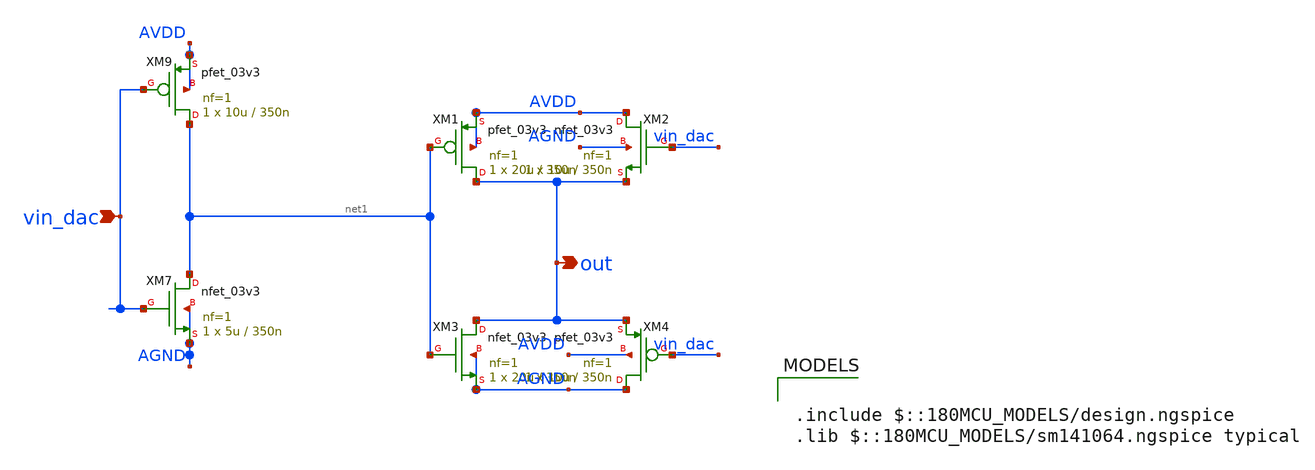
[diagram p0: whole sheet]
** sch_path: untitled.sch
**.subckt untitled vin_dac out
*.ipin vin_dac
*.opin out
XM7 net1 vin_dac AGND AGND nfet_03v3 L=350n W=5u nf=1 ad='int((nf+1)/2) * W/nf * 0.18u' as='int((nf+2)/2) * W/nf * 0.18u'
+ pd='2*int((nf+1)/2) * (W/nf + 0.18u)' ps='2*int((nf+2)/2) * (W/nf + 0.18u)' nrd='0.18u / W' nrs='0.18u / W'
+ sa=0 sb=0 sd=0 m=1
XM9 net1 vin_dac AVDD AVDD pfet_03v3 L=350n W=10u nf=1 ad='int((nf+1)/2) * W/nf * 0.18u' as='int((nf+2)/2) * W/nf * 0.18u'
+ pd='2*int((nf+1)/2) * (W/nf + 0.18u)' ps='2*int((nf+2)/2) * (W/nf + 0.18u)' nrd='0.18u / W' nrs='0.18u / W'
+ sa=0 sb=0 sd=0 m=1
XM1 out net1 AVDD AVDD pfet_03v3 L=350n W=20u nf=1 ad='int((nf+1)/2) * W/nf * 0.18u' as='int((nf+2)/2) * W/nf * 0.18u'
+ pd='2*int((nf+1)/2) * (W/nf + 0.18u)' ps='2*int((nf+2)/2) * (W/nf + 0.18u)' nrd='0.18u / W' nrs='0.18u / W'
+ sa=0 sb=0 sd=0 m=1
XM2 AVDD vin_dac out AGND nfet_03v3 L=350n W=10u nf=1 ad='int((nf+1)/2) * W/nf * 0.18u' as='int((nf+2)/2) * W/nf * 0.18u'
+ pd='2*int((nf+1)/2) * (W/nf + 0.18u)' ps='2*int((nf+2)/2) * (W/nf + 0.18u)' nrd='0.18u / W' nrs='0.18u / W'
+ sa=0 sb=0 sd=0 m=1
XM3 out net1 AGND AGND nfet_03v3 L=350n W=20u nf=1 ad='int((nf+1)/2) * W/nf * 0.18u' as='int((nf+2)/2) * W/nf * 0.18u'
+ pd='2*int((nf+1)/2) * (W/nf + 0.18u)' ps='2*int((nf+2)/2) * (W/nf + 0.18u)' nrd='0.18u / W' nrs='0.18u / W'
+ sa=0 sb=0 sd=0 m=1
XM4 AGND vin_dac out AVDD pfet_03v3 L=350n W=10u nf=1 ad='int((nf+1)/2) * W/nf * 0.18u' as='int((nf+2)/2) * W/nf * 0.18u'
+ pd='2*int((nf+1)/2) * (W/nf + 0.18u)' ps='2*int((nf+2)/2) * (W/nf + 0.18u)' nrd='0.18u / W' nrs='0.18u / W'
+ sa=0 sb=0 sd=0 m=1
**** begin user architecture code

.include $::180MCU_MODELS/design.ngspice
.lib $::180MCU_MODELS/sm141064.ngspice typical

**** end user architecture code
**.ends
.end
